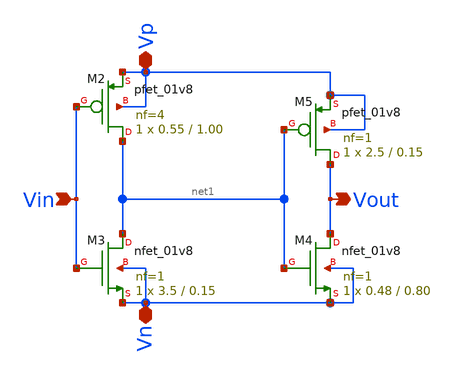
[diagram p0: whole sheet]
** sch_path: xschem/Vth_sch/Symbol/th01_1.sch
**.subckt th01_1 Vin Vout Vp Vn
*.ipin Vin
*.opin Vout
*.iopin Vp
*.iopin Vn
XM5 Vout net1 Vp Vp sky130_fd_pr__pfet_01v8 L=0.15 W=2.5 nf=1 ad='int((nf+1)/2) * W/nf * 0.29' as='int((nf+2)/2) * W/nf * 0.29'
+ pd='2*int((nf+1)/2) * (W/nf + 0.29)' ps='2*int((nf+2)/2) * (W/nf + 0.29)' nrd='0.29 / W' nrs='0.29 / W'
+ sa=0 sb=0 sd=0 mult=1 m=1
XM4 Vout net1 Vn Vn sky130_fd_pr__nfet_01v8 L=0.80 W=0.48 nf=1 ad='int((nf+1)/2) * W/nf * 0.29' as='int((nf+2)/2) * W/nf * 0.29'
+ pd='2*int((nf+1)/2) * (W/nf + 0.29)' ps='2*int((nf+2)/2) * (W/nf + 0.29)' nrd='0.29 / W' nrs='0.29 / W'
+ sa=0 sb=0 sd=0 mult=1 m=1
XM2 net1 Vin Vp Vp sky130_fd_pr__pfet_01v8 L=1.00 W=0.55 nf=4 ad='int((nf+1)/2) * W/nf * 0.29' as='int((nf+2)/2) * W/nf * 0.29'
+ pd='2*int((nf+1)/2) * (W/nf + 0.29)' ps='2*int((nf+2)/2) * (W/nf + 0.29)' nrd='0.29 / W' nrs='0.29 / W'
+ sa=0 sb=0 sd=0 mult=1 m=1
XM3 net1 Vin Vn Vn sky130_fd_pr__nfet_01v8 L=0.15 W=3.5 nf=1 ad='int((nf+1)/2) * W/nf * 0.29' as='int((nf+2)/2) * W/nf * 0.29'
+ pd='2*int((nf+1)/2) * (W/nf + 0.29)' ps='2*int((nf+2)/2) * (W/nf + 0.29)' nrd='0.29 / W' nrs='0.29 / W'
+ sa=0 sb=0 sd=0 mult=1 m=1
**.ends
.end
